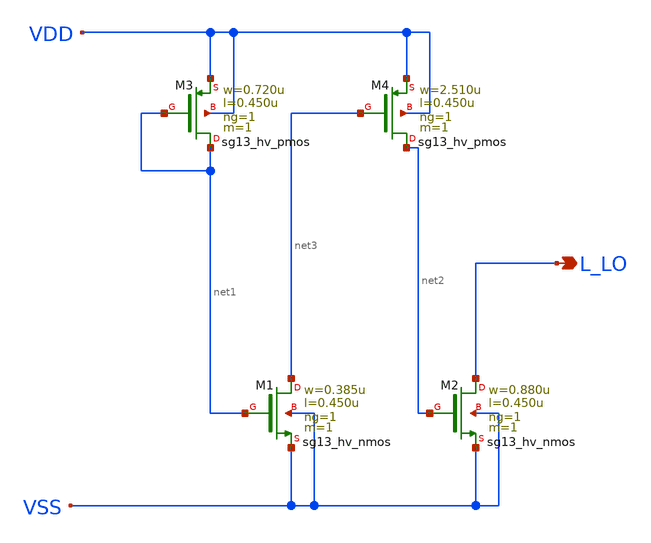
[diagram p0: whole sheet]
** sch_path: sch/xschem/sg13g2_hv_tielo.sch
* Copyright 2023 IHP PDK Authors
* Licensed under the Apache License, Version 2.0 (the "License");
* you may not use this file except in compliance with the License.
* You may obtain a copy of the License at
* https://www.apache.org/licenses/LICENSE-2.0
* Unless required by applicable law or agreed to in writing, software
* distributed under the License is distributed on an "AS IS" BASIS,
* WITHOUT WARRANTIES OR CONDITIONS OF ANY KIND, either express or implied.
* See the License for the specific language governing permissions and
* limitations under the License.
**.subckt sg13g2_hv_tielo L_LO
*.opin L_LO
XM1 net3 net1 VSS VSS sg13_hv_nmos w=0.385u l=0.450u ng=1 m=1 mm_ok=1
XM2 L_LO net2 VSS VSS sg13_hv_nmos w=0.880u l=0.450u ng=1 m=1 mm_ok=1
XM3 net1 net1 VDD VDD sg13_hv_pmos w=0.720u l=0.450u ng=1 m=1 mm_ok=1
XM4 net2 net3 VDD VDD sg13_hv_pmos w=2.510u l=0.450u ng=1 m=1 mm_ok=1
**.ends
.end
